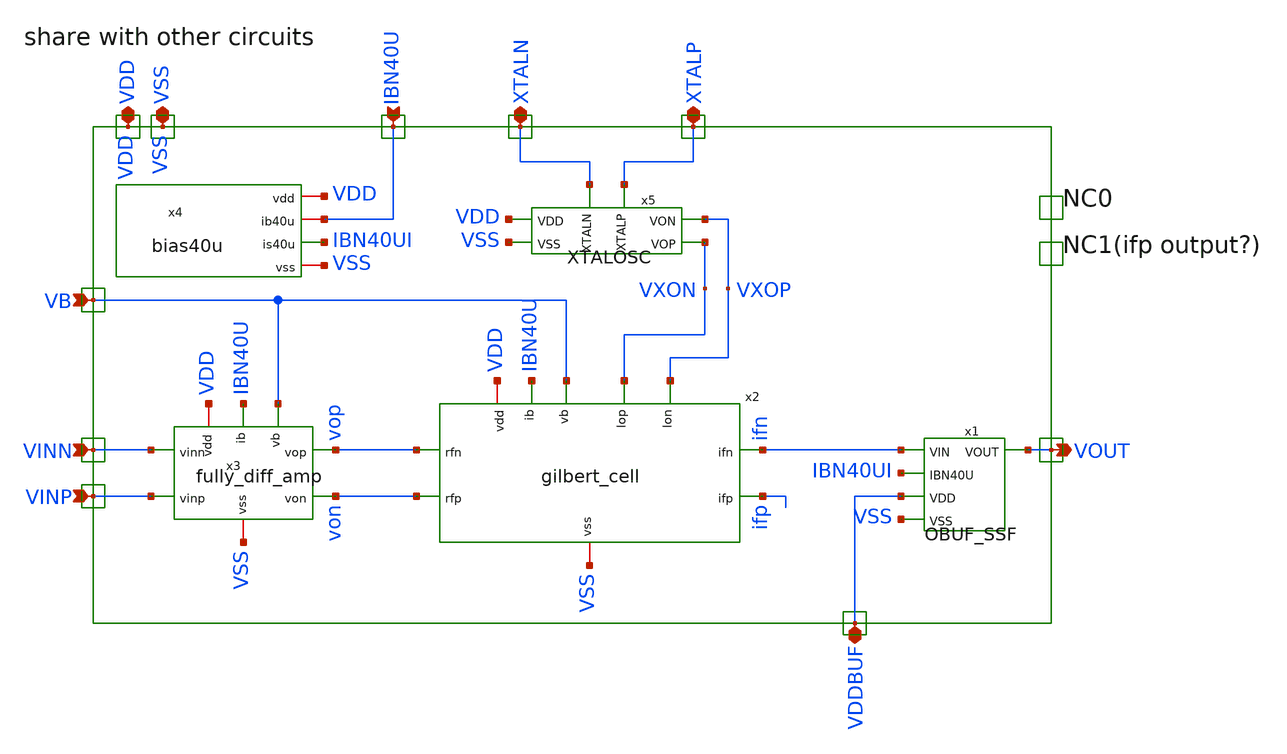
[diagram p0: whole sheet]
** sch_path: member_project/JJY_Receiver/Masahiro/jjy_recv/top/top.sch
**.subckt top IBN40U XTALN VINN XTALP VINP VB VDD VOUT VDDBUF VSS
*.ipin IBN40U
*.iopin XTALN
*.ipin VINN
*.iopin XTALP
*.ipin VINP
*.ipin VB
*.iopin VDD
*.opin VOUT
*.iopin VDDBUF
*.iopin VSS
x2 VB ifn VDD ifp VSS VXON VXOP vop von IBN40U gilbert_cell
x3 VB VDD vop von VSS VINN VINP IBN40U fully_diff_amp
x1 VDDBUF VSS ifn VOUT IBN40UI OBUF_SSF
x4 VDD IBN40U IBN40UI VSS bias40u
x5 VDD VSS VXOP XTALN XTALP VXON XTALOSC
**.ends
.end
